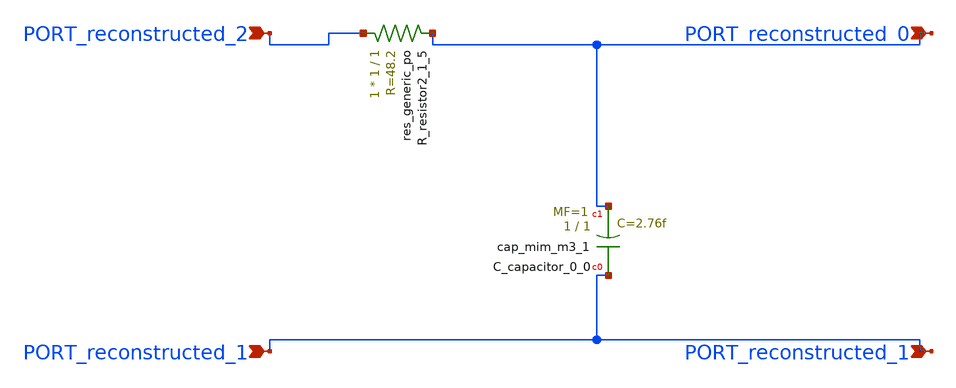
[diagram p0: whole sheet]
** sch_path: schematics/AMSNet/685.sch
**.subckt 685 PORT_reconstructed_1 PORT_reconstructed_2 PORT_reconstructed_0 PORT_reconstructed_1
*.ipin PORT_reconstructed_1
*.ipin PORT_reconstructed_2
*.ipin PORT_reconstructed_0
*.ipin PORT_reconstructed_1
XC_capacitor_0_0 PORT_reconstructed_1 PORT_reconstructed_0 sky130_fd_pr__cap_mim_m3_1 W=1 L=1 MF=1
+ m=1
XR_resistor2_1_5 PORT_reconstructed_2 PORT_reconstructed_0 sky130_fd_pr__res_generic_po W=1 L=1 m=1
**.ends
.end
